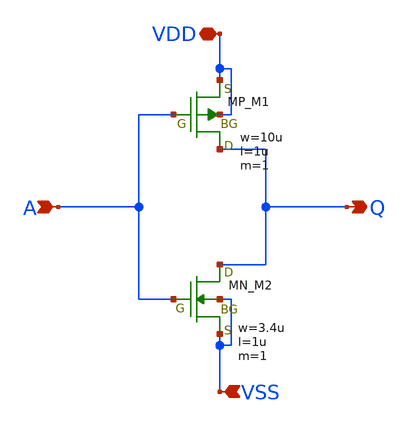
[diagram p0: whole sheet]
** sch_path: member_project/inverter/ZEP/makoto645/inverter_makoto645.sch
**.subckt inverter_makoto645 VDD VSS A Q
*.iopin VDD
*.ipin VSS
*.ipin A
*.opin Q
XM1 Q A VDD VDD PMOS w=10u l=1u as=0 ad=0 ps=0 pd=0 nrd=0 nrs=0 m=1
XM2 Q A VSS VSS NMOS w=3.4u l=1u as=0 ad=0 ps=0 pd=0 nrd=0 nrs=0 m=1
**.ends
.end
